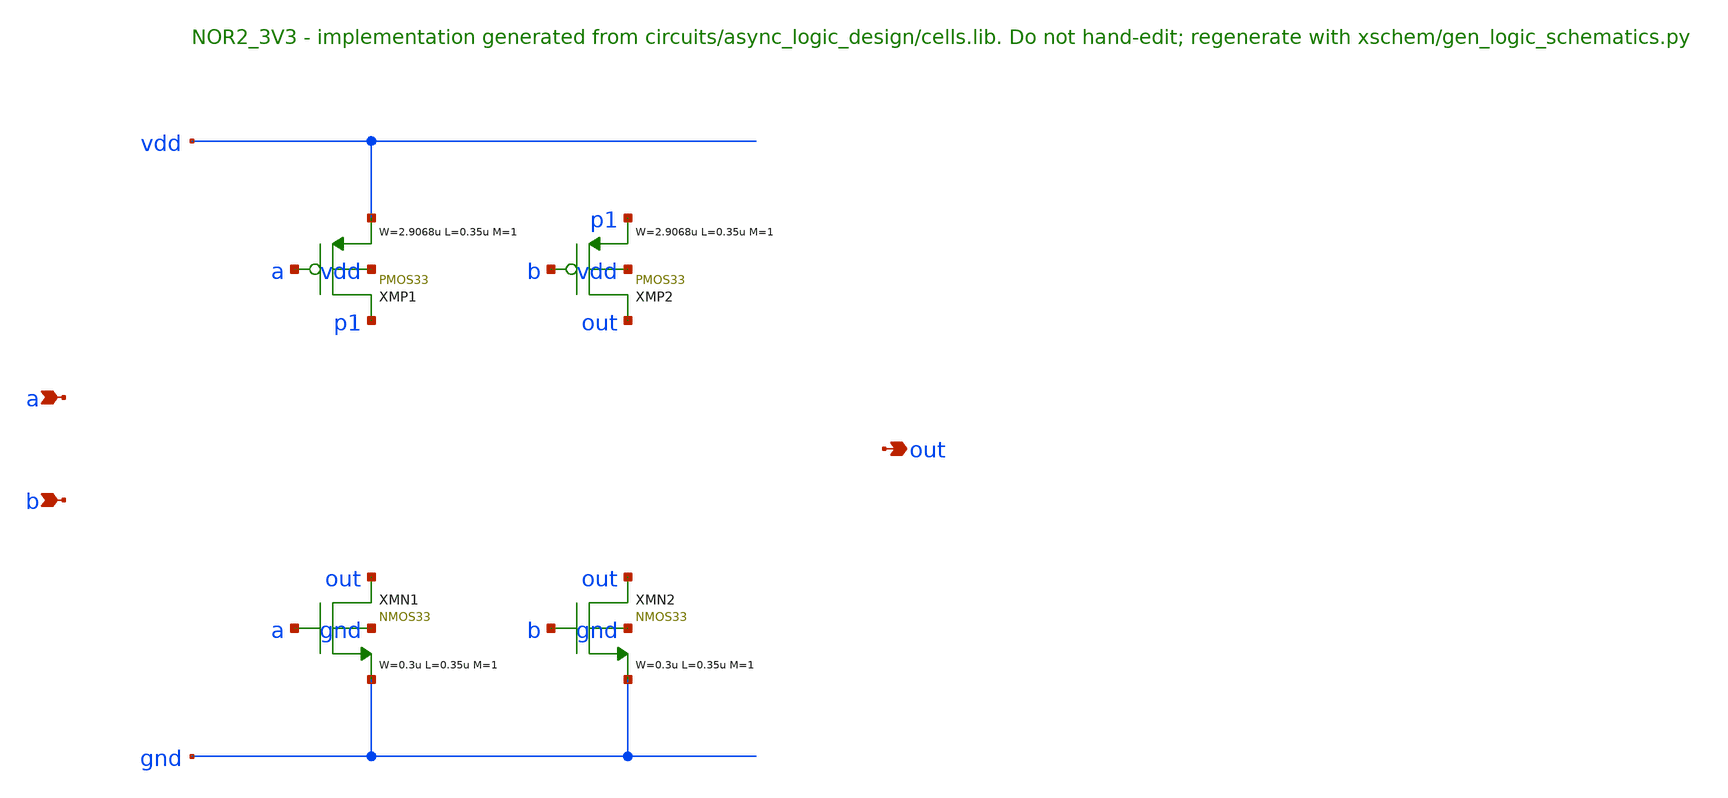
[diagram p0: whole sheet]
** sch_path: xschem/logic/NOR2_3V3.sch
**.subckt NOR2_3V3 a b out
*.ipin a
*.ipin b
*.opin out
XMP1 p1 a vdd vdd PMOS33 W=2.9068u L=0.35u M=1 MM_SIGMA=0
XMP2 out b p1 vdd PMOS33 W=2.9068u L=0.35u M=1 MM_SIGMA=0
XMN1 out a gnd gnd NMOS33 W=0.3u L=0.35u M=1 MM_SIGMA=0
XMN2 out b gnd gnd NMOS33 W=0.3u L=0.35u M=1 MM_SIGMA=0
**.ends
.end
